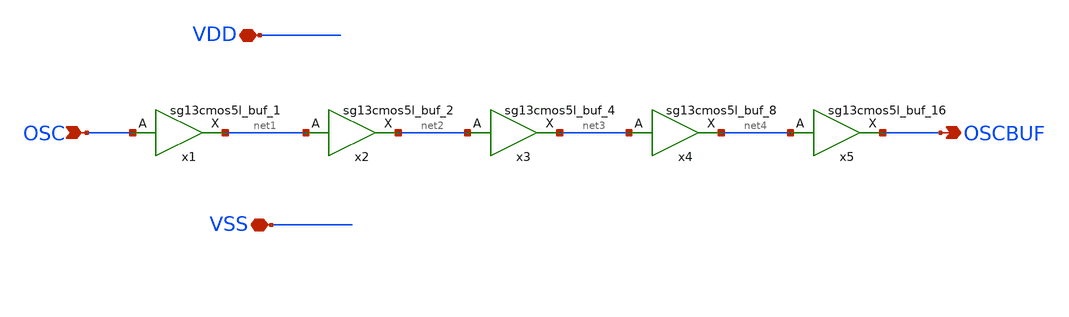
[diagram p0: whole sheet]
** sch_path: MPU9547-main/analog/schematic/OSCBUFOUT.sch
**.subckt OSCBUFOUT OSC VDD VSS OSCBUF
*.ipin OSC
*.iopin VDD
*.iopin VSS
*.opin OSCBUF
x1 net1 OSC VDD VSS sg13cmos5l_buf_1
x3 net3 net2 VDD VSS sg13cmos5l_buf_4
x4 net4 net3 VDD VSS sg13cmos5l_buf_8
x5 OSCBUF net4 VDD VSS sg13cmos5l_buf_16
x2 net2 net1 VDD VSS sg13cmos5l_buf_2
**.ends
.end
